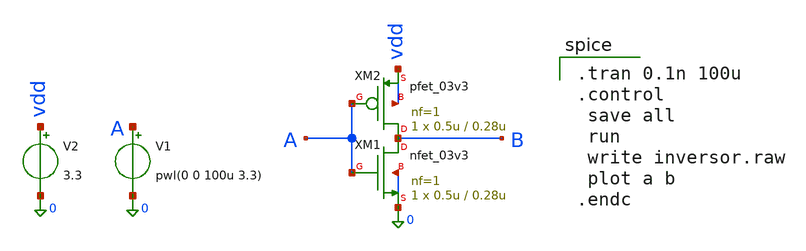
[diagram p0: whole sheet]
** sch_path: sim_postlayout/esquematicos/inversor.sch
**.subckt inversor
XM1 B A 0 0 nfet_03v3 L=0.28u W=0.5u nf=1 ad='int((nf+1)/2) * W/nf * 0.18u' as='int((nf+2)/2) * W/nf * 0.18u'
+ pd='2*int((nf+1)/2) * (W/nf + 0.18u)' ps='2*int((nf+2)/2) * (W/nf + 0.18u)' nrd='0.18u / W' nrs='0.18u / W'
+ sa=0 sb=0 sd=0 m=1 par=1
XM2 B A vdd vdd pfet_03v3 L=0.28u W=0.5u nf=1 ad='int((nf+1)/2) * W/nf * 0.18u' as='int((nf+2)/2) * W/nf * 0.18u'
+ pd='2*int((nf+1)/2) * (W/nf + 0.18u)' ps='2*int((nf+2)/2) * (W/nf + 0.18u)' nrd='0.18u / W' nrs='0.18u / W'
+ sa=0 sb=0 sd=0 m=1 par=1
V1 A 0 pwl(0 0 100u 3.3)
V2 vdd 0 3.3
**** begin user architecture code

.include $::180MCU_MODELS/design.ngspice
.lib $::180MCU_MODELS/sm141064.ngspice typical


.tran 0.1n 100u
.control
 save all
 run
 write inversor.raw
 plot a b
.endc

**** end user architecture code
**.ends
.end
